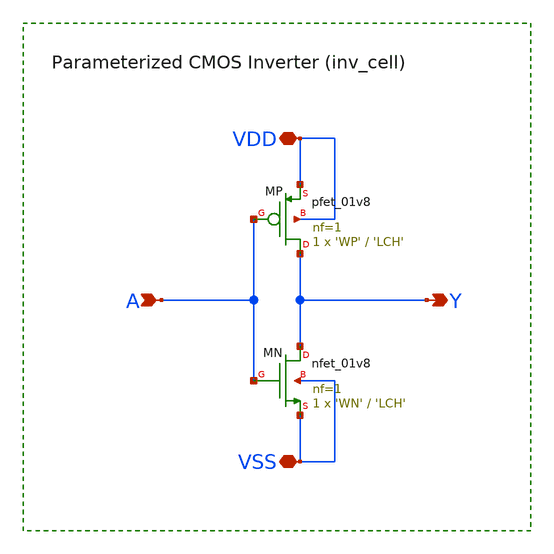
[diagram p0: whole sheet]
** sch_path: sky130-sc-lpf/xschem/inv_cell.sch
**.subckt inv_cell A Y VDD VSS
*.ipin A
*.opin Y
*.iopin VDD
*.iopin VSS
XMP Y A VDD VDD sky130_fd_pr__pfet_01v8 L='LCH' W='WP' nf=1 ad='WP*0.29' as='WP*0.29' pd='2*(WP+0.29)'
+ ps='2*(WP+0.29)' nrd='0.29/WP' nrs='0.29/WP' sa=0 sb=0 sd=0 mult=1 m=1
XMN Y A VSS VSS sky130_fd_pr__nfet_01v8 L='LCH' W='WN' nf=1 ad='WN*0.29' as='WN*0.29' pd='2*(WN+0.29)'
+ ps='2*(WN+0.29)' nrd='0.29/WN' nrs='0.29/WN' sa=0 sb=0 sd=0 mult=1 m=1
**.ends
.end
